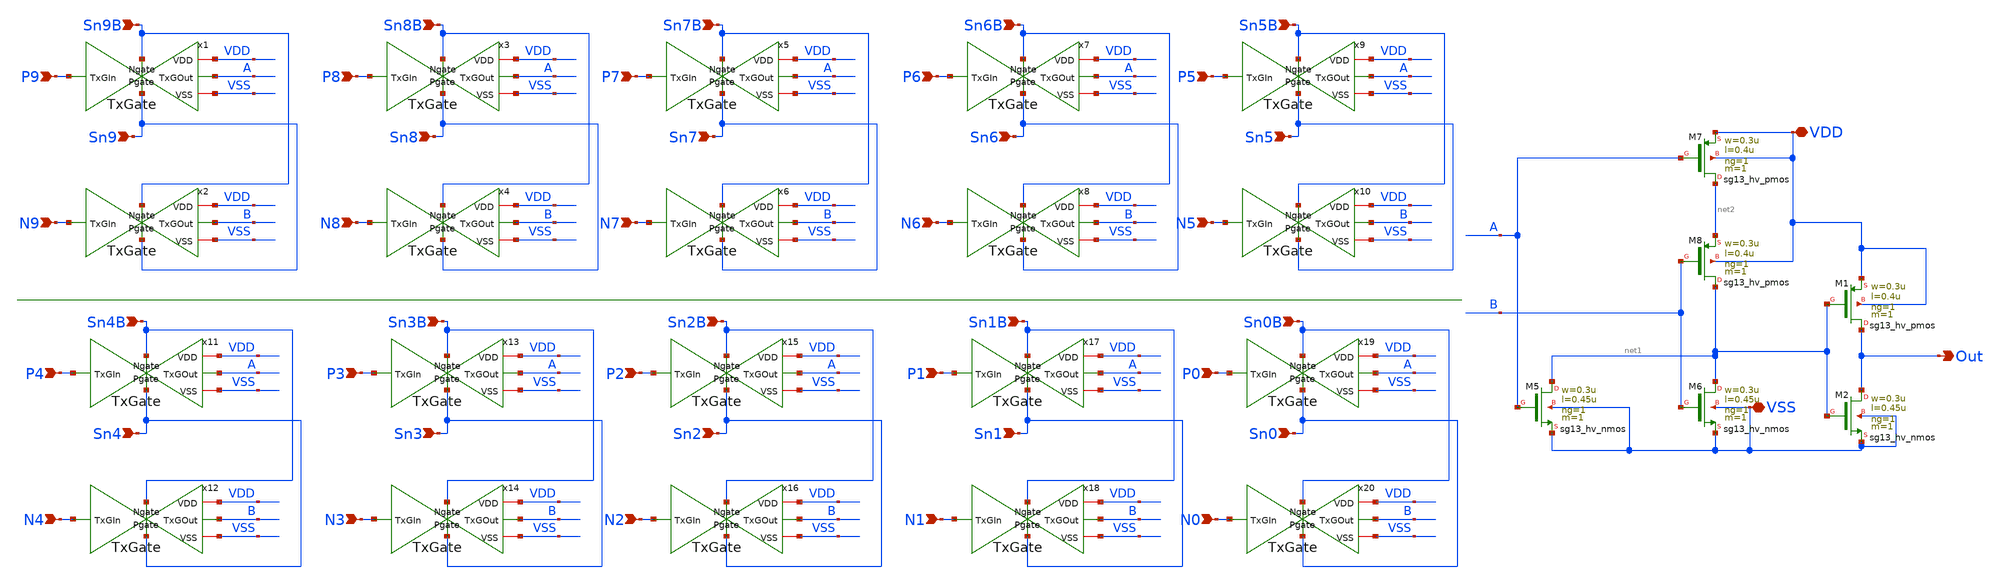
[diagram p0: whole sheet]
** sch_path: circuit_files/sar_adc_20260903/cdacSettleCheck.sch
**.subckt cdacSettleCheck Sn9B P9 N9 Sn8B Sn8 P8 N8 Sn7B Sn7 P7 N7 Sn6B Sn6 P6 N6 Sn5B Sn5 P5 N5
*+ Sn4B Sn4 P4 N4 Sn3B Sn3 P3 N3 Sn2B Sn2 P2 N2 Sn1B Sn1 P1 N1 Sn0B Sn0 P0 N0 VDD VSS Sn9 Out
*.ipin Sn9B
*.ipin P9
*.ipin N9
*.ipin Sn8B
*.ipin Sn8
*.ipin P8
*.ipin N8
*.ipin Sn7B
*.ipin Sn7
*.ipin P7
*.ipin N7
*.ipin Sn6B
*.ipin Sn6
*.ipin P6
*.ipin N6
*.ipin Sn5B
*.ipin Sn5
*.ipin P5
*.ipin N5
*.ipin Sn4B
*.ipin Sn4
*.ipin P4
*.ipin N4
*.ipin Sn3B
*.ipin Sn3
*.ipin P3
*.ipin N3
*.ipin Sn2B
*.ipin Sn2
*.ipin P2
*.ipin N2
*.ipin Sn1B
*.ipin Sn1
*.ipin P1
*.ipin N1
*.ipin Sn0B
*.ipin Sn0
*.ipin P0
*.ipin N0
*.iopin VDD
*.iopin VSS
*.ipin Sn9
*.opin Out
XM5 net1 A VSS VSS sg13_hv_nmos w=0.3u l=0.45u ng=1 m=1 mm_ok=1
XM6 net1 B VSS VSS sg13_hv_nmos w=0.3u l=0.45u ng=1 m=1 mm_ok=1
XM7 net2 A VDD VDD sg13_hv_pmos w=0.3u l=0.4u ng=1 m=1 mm_ok=1
XM8 net1 B net2 VDD sg13_hv_pmos w=0.3u l=0.4u ng=1 m=1 mm_ok=1
x1 Sn9B VDD P9 A VSS Sn9 TxGate
x2 Sn9B VDD N9 B VSS Sn9 TxGate
x3 Sn8B VDD P8 A VSS Sn8 TxGate
x4 Sn8B VDD N8 B VSS Sn8 TxGate
x5 Sn7B VDD P7 A VSS Sn7 TxGate
x6 Sn7B VDD N7 B VSS Sn7 TxGate
x7 Sn6B VDD P6 A VSS Sn6 TxGate
x8 Sn6B VDD N6 B VSS Sn6 TxGate
x9 Sn5B VDD P5 A VSS Sn5 TxGate
x10 Sn5B VDD N5 B VSS Sn5 TxGate
x11 Sn4B VDD P4 A VSS Sn4 TxGate
x12 Sn4B VDD N4 B VSS Sn4 TxGate
x13 Sn3B VDD P3 A VSS Sn3 TxGate
x14 Sn3B VDD N3 B VSS Sn3 TxGate
x15 Sn2B VDD P2 A VSS Sn2 TxGate
x16 Sn2B VDD N2 B VSS Sn2 TxGate
x17 Sn1B VDD P1 A VSS Sn1 TxGate
x18 Sn1B VDD N1 B VSS Sn1 TxGate
x19 Sn0B VDD P0 A VSS Sn0 TxGate
x20 Sn0B VDD N0 B VSS Sn0 TxGate
XM1 Out net1 VDD VDD sg13_hv_pmos w=0.3u l=0.4u ng=1 m=1 mm_ok=1
XM2 Out net1 VSS VSS sg13_hv_nmos w=0.3u l=0.45u ng=1 m=1 mm_ok=1
**.ends

* expanding   symbol:  /foss/designs/sarADC/sar_adc_20260903/TxGate.sym # of pins=6
** sym_path: circuit_files/xschem_symbols/TxGate.sym
** sch_path: circuit_files/xschem_symbols/TxGate.sch
.subckt TxGate Ngate VDD TxGIn TxGOut VSS Pgate
*.ipin Ngate
*.ipin Pgate
*.ipin TxGIn
*.opin TxGOut
*.iopin VDD
*.iopin VSS
XM13 TxGOut Ngate net1 VSS sg13_lv_nmos w=0.15u l=0.13u ng=1 m=1 mm_ok=1
XM14 TxGOut Pgate net1 VDD sg13_lv_pmos w=0.15u l=0.13u ng=1 m=1 mm_ok=1
XM1 net1 net2 VSS VSS sg13_lv_nmos w=0.15u l=0.13u ng=1 m=1 mm_ok=1
XM2 net1 net2 VDD VDD sg13_lv_pmos w=0.15u l=0.13u ng=1 m=1 mm_ok=1
XM3 net2 TxGIn VSS VSS sg13_lv_nmos w=0.15u l=0.13u ng=1 m=1 mm_ok=1
XM4 net2 TxGIn VDD VDD sg13_lv_pmos w=0.15u l=0.13u ng=1 m=1 mm_ok=1
.ends

.end
